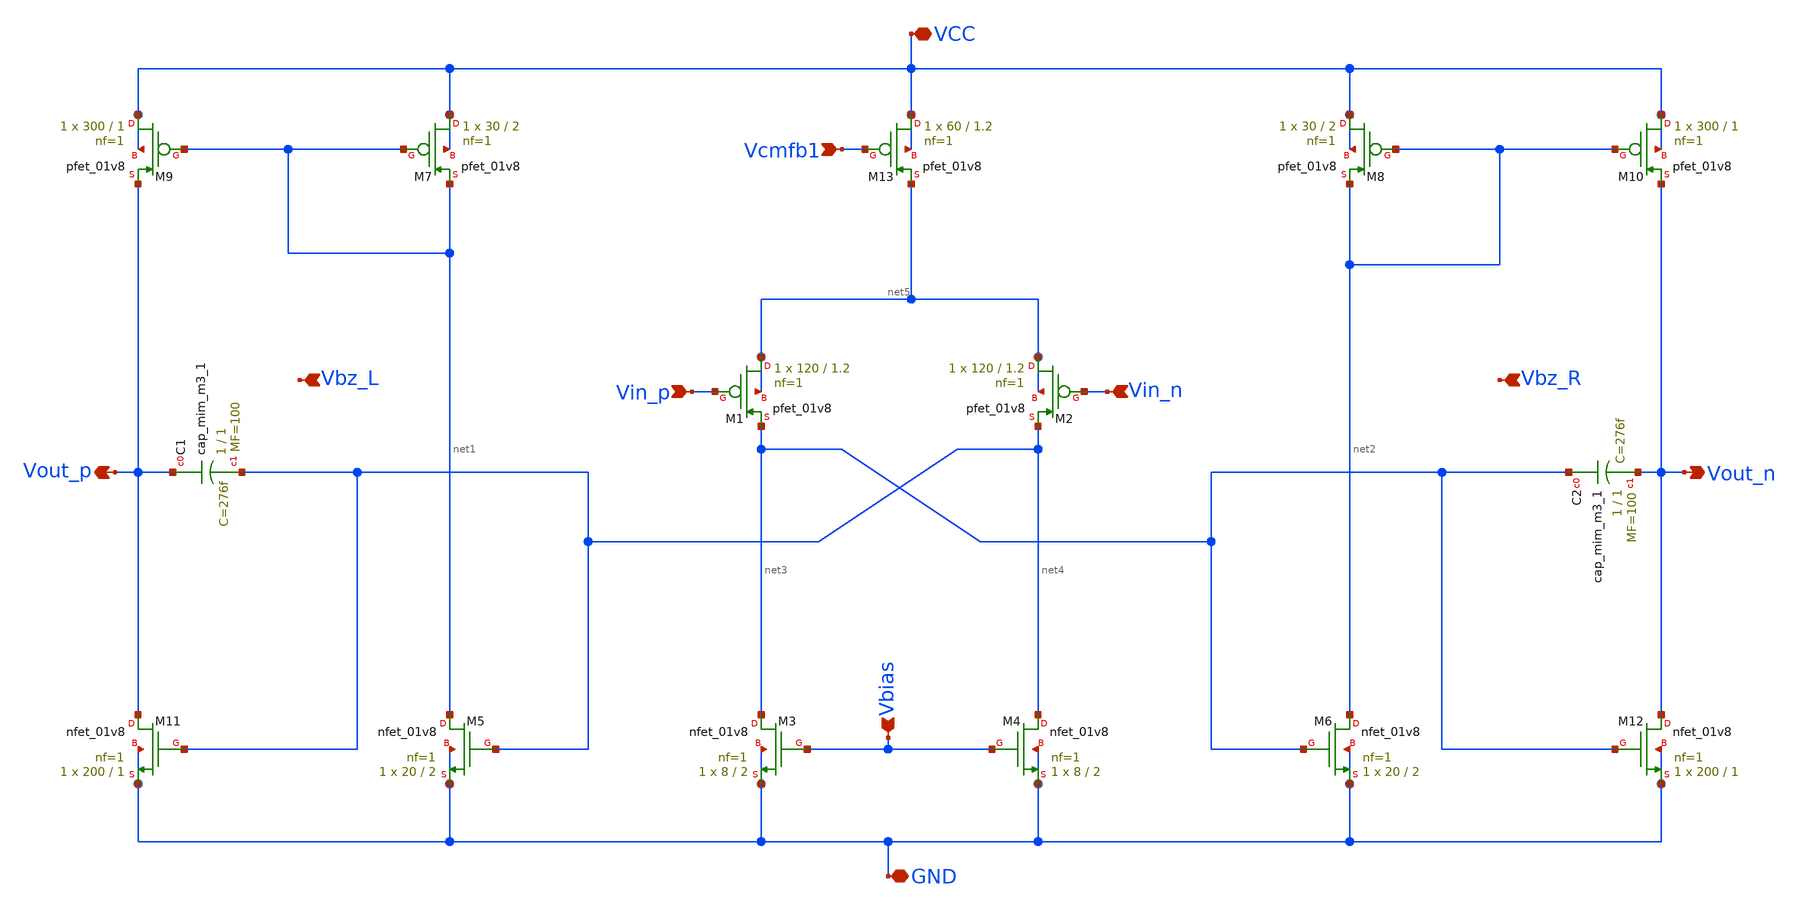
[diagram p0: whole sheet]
** sch_path: blocks/01_OTA/xschem/OTA_experiment_MF100.sch
**.subckt OTA_experiment_MF100 Vin_p Vin_n Vbias Vbz_R Vbz_L Vcmfb1 Vout_p Vout_n VCC GND
*.ipin Vin_p
*.ipin Vin_n
*.ipin Vbias
*.ipin Vbz_R
*.ipin Vbz_L
*.ipin Vcmfb1
*.opin Vout_p
*.opin Vout_n
*.iopin VCC
*.iopin GND
XM1 net5 Vin_p net3 net5 sky130_fd_pr__pfet_01v8 L=1.2 W=120 nf=1 ad='int((1 + 1)/2) * 120 / 1 * 0.29'
+ as='int((1 + 2)/2) * 120 / 1 * 0.29' pd='2*int((1 + 1)/2) * (120 / 1 + 0.29)' ps='2*int((1 + 2)/2) * (120 / 1 + 0.29)'
+ nrd='0.29 / 120 ' nrs='0.29 / 120 ' sa=0 sb=0 sd=0 mult=1 m=1
XM2 net5 Vin_n net4 net5 sky130_fd_pr__pfet_01v8 L=1.2 W=120 nf=1 ad='int((1 + 1)/2) * 120 / 1 * 0.29'
+ as='int((1 + 2)/2) * 120 / 1 * 0.29' pd='2*int((1 + 1)/2) * (120 / 1 + 0.29)' ps='2*int((1 + 2)/2) * (120 / 1 + 0.29)'
+ nrd='0.29 / 120 ' nrs='0.29 / 120 ' sa=0 sb=0 sd=0 mult=1 m=1
XM3 net3 Vbias GND GND sky130_fd_pr__nfet_01v8 L=2 W=8 nf=1 ad='int((1 + 1)/2) * 8 / 1 * 0.29' as='int((1 + 2)/2) * 8 / 1 * 0.29'
+ pd='2*int((1 + 1)/2) * (8 / 1 + 0.29)' ps='2*int((1 + 2)/2) * (8 / 1 + 0.29)' nrd='0.29 / 8 ' nrs='0.29 / 8 '
+ sa=0 sb=0 sd=0 mult=1 m=1
XM4 net4 Vbias GND GND sky130_fd_pr__nfet_01v8 L=2 W=8 nf=1 ad='int((1 + 1)/2) * 8 / 1 * 0.29' as='int((1 + 2)/2) * 8 / 1 * 0.29'
+ pd='2*int((1 + 1)/2) * (8 / 1 + 0.29)' ps='2*int((1 + 2)/2) * (8 / 1 + 0.29)' nrd='0.29 / 8 ' nrs='0.29 / 8 '
+ sa=0 sb=0 sd=0 mult=1 m=1
XM5 net1 net4 GND GND sky130_fd_pr__nfet_01v8 L=2 W=20 nf=1 ad='int((1 + 1)/2) * 20 / 1 * 0.29' as='int((1 + 2)/2) * 20 / 1 * 0.29'
+ pd='2*int((1 + 1)/2) * (20 / 1 + 0.29)' ps='2*int((1 + 2)/2) * (20 / 1 + 0.29)' nrd='0.29 / 20 ' nrs='0.29 / 20 '
+ sa=0 sb=0 sd=0 mult=1 m=1
XM6 net2 net3 GND GND sky130_fd_pr__nfet_01v8 L=2 W=20 nf=1 ad='int((1 + 1)/2) * 20 / 1 * 0.29' as='int((1 + 2)/2) * 20 / 1 * 0.29'
+ pd='2*int((1 + 1)/2) * (20 / 1 + 0.29)' ps='2*int((1 + 2)/2) * (20 / 1 + 0.29)' nrd='0.29 / 20 ' nrs='0.29 / 20 '
+ sa=0 sb=0 sd=0 mult=1 m=1
XM7 VCC net1 net1 VCC sky130_fd_pr__pfet_01v8 L=2 W=30 nf=1 ad='int((1 + 1)/2) * 30 / 1 * 0.29' as='int((1 + 2)/2) * 30 / 1 * 0.29'
+ pd='2*int((1 + 1)/2) * (30 / 1 + 0.29)' ps='2*int((1 + 2)/2) * (30 / 1 + 0.29)' nrd='0.29 / 30 ' nrs='0.29 / 30 '
+ sa=0 sb=0 sd=0 mult=1 m=1
XM8 VCC net2 net2 VCC sky130_fd_pr__pfet_01v8 L=2 W=30 nf=1 ad='int((1 + 1)/2) * 30 / 1 * 0.29' as='int((1 + 2)/2) * 30 / 1 * 0.29'
+ pd='2*int((1 + 1)/2) * (30 / 1 + 0.29)' ps='2*int((1 + 2)/2) * (30 / 1 + 0.29)' nrd='0.29 / 30 ' nrs='0.29 / 30 '
+ sa=0 sb=0 sd=0 mult=1 m=1
XM9 VCC net1 Vout_p VCC sky130_fd_pr__pfet_01v8 L=1 W=300 nf=1 ad='int((1 + 1)/2) * 300 / 1 * 0.29' as='int((1 + 2)/2) * 300 / 1 * 0.29'
+ pd='2*int((1 + 1)/2) * (300 / 1 + 0.29)' ps='2*int((1 + 2)/2) * (300 / 1 + 0.29)' nrd='0.29 / 300 ' nrs='0.29 / 300 '
+ sa=0 sb=0 sd=0 mult=1 m=1
XM10 VCC net2 Vout_n VCC sky130_fd_pr__pfet_01v8 L=1 W=300 nf=1 ad='int((1 + 1)/2) * 300 / 1 * 0.29'
+ as='int((1 + 2)/2) * 300 / 1 * 0.29' pd='2*int((1 + 1)/2) * (300 / 1 + 0.29)' ps='2*int((1 + 2)/2) * (300 / 1 + 0.29)'
+ nrd='0.29 / 300 ' nrs='0.29 / 300 ' sa=0 sb=0 sd=0 mult=1 m=1
XM11 Vout_p net4 GND GND sky130_fd_pr__nfet_01v8 L=1 W=200 nf=1 ad='int((1 + 1)/2) * 200 / 1 * 0.29'
+ as='int((1 + 2)/2) * 200 / 1 * 0.29' pd='2*int((1 + 1)/2) * (200 / 1 + 0.29)' ps='2*int((1 + 2)/2) * (200 / 1 + 0.29)'
+ nrd='0.29 / 200 ' nrs='0.29 / 200 ' sa=0 sb=0 sd=0 mult=1 m=1
XM12 Vout_n net3 GND GND sky130_fd_pr__nfet_01v8 L=1 W=200 nf=1 ad='int((1 + 1)/2) * 200 / 1 * 0.29'
+ as='int((1 + 2)/2) * 200 / 1 * 0.29' pd='2*int((1 + 1)/2) * (200 / 1 + 0.29)' ps='2*int((1 + 2)/2) * (200 / 1 + 0.29)'
+ nrd='0.29 / 200 ' nrs='0.29 / 200 ' sa=0 sb=0 sd=0 mult=1 m=1
XM13 VCC Vcmfb1 net5 VCC sky130_fd_pr__pfet_01v8 L=1.2 W=60 nf=1 ad='int((1 + 1)/2) * 60 / 1 * 0.29'
+ as='int((1 + 2)/2) * 60 / 1 * 0.29' pd='2*int((1 + 1)/2) * (60 / 1 + 0.29)' ps='2*int((1 + 2)/2) * (60 / 1 + 0.29)'
+ nrd='0.29 / 60 ' nrs='0.29 / 60 ' sa=0 sb=0 sd=0 mult=1 m=1
XC1 Vout_p net4 sky130_fd_pr__cap_mim_m3_1 W=1 L=1 MF=100 m=100
XC2 net3 Vout_n sky130_fd_pr__cap_mim_m3_1 W=1 L=1 MF=100 m=100
**.ends
.end
